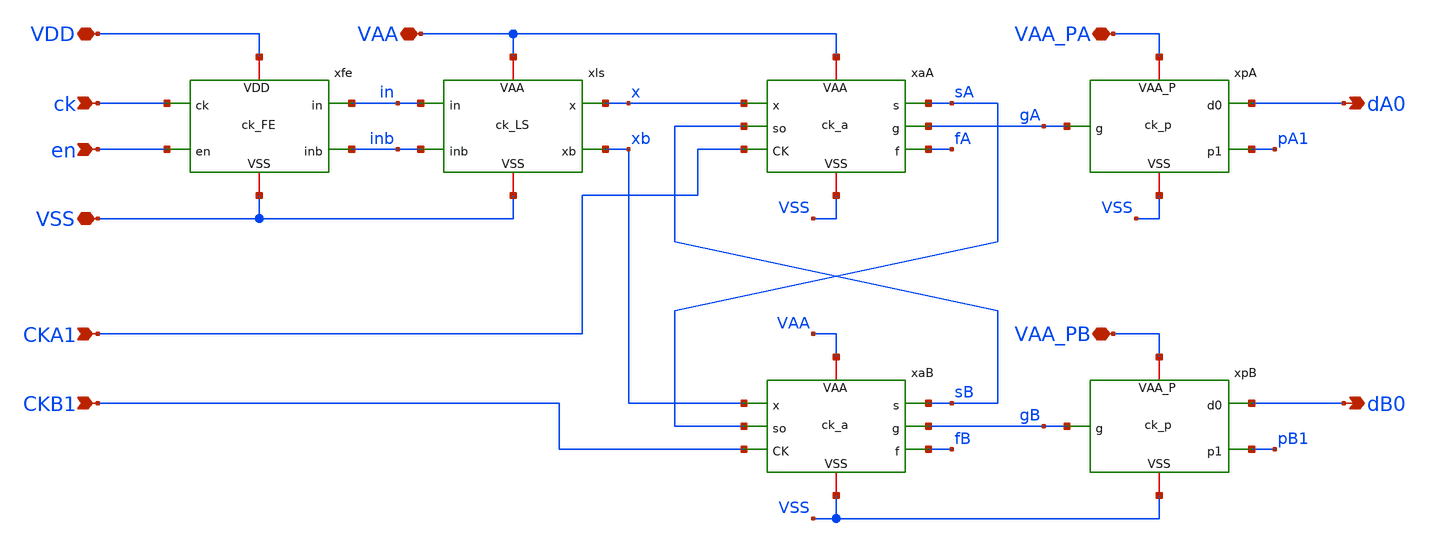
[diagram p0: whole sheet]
** sch_path: xschem/clkblock.sch
**.subckt clkblock VSS dA0 dB0 ck en VDD VAA VAA_PA VAA_PB CKA1 CKB1
*.iopin VSS
*.opin dA0
*.opin dB0
*.ipin ck
*.ipin en
*.iopin VDD
*.iopin VAA
*.iopin VAA_PA
*.iopin VAA_PB
*.ipin CKA1
*.ipin CKB1
xfe ck en inb in VSS VDD ck_FE
xls in inb x xb VSS VAA ck_LS
xaA gA sB x CKA1 fA sA VSS VAA ck_a
xaB gB sA xb CKB1 fB sB VSS VAA ck_a
xpA gA pA1 dA0 VSS VAA_PA ck_p
xpB gB pB1 dB0 VSS VAA_PB ck_p
**.ends

* expanding   symbol:  ck_FE.sym # of pins=6
** sym_path: xschem/ck_FE.sym
** sch_path: xschem/ck_FE.sch
.subckt ck_FE ck en inb in VSS VDD
*.iopin VDD
*.iopin VSS
*.ipin ck
*.ipin en
*.opin in
*.opin inb
XPN1 inb ck VDD VDD pfet_03v3 L=1.12u W=2.0u nf=1 ad='int((nf+1)/2) * W/nf * 0.18u' as='int((nf+2)/2) * W/nf * 0.18u'
+ pd='2*int((nf+1)/2) * (W/nf + 0.18u)' ps='2*int((nf+2)/2) * (W/nf + 0.18u)' nrd='0.18u / W' nrs='0.18u / W'
+ sa=0 sb=0 sd=0 m=1 par=1
XPN2 inb en VDD VDD pfet_03v3 L=1.12u W=2.0u nf=1 ad='int((nf+1)/2) * W/nf * 0.18u' as='int((nf+2)/2) * W/nf * 0.18u'
+ pd='2*int((nf+1)/2) * (W/nf + 0.18u)' ps='2*int((nf+2)/2) * (W/nf + 0.18u)' nrd='0.18u / W' nrs='0.18u / W'
+ sa=0 sb=0 sd=0 m=1 par=1
XNN1 inb ck nn VSS nfet_03v3 L=1.12u W=2.0u nf=1 ad='int((nf+1)/2) * W/nf * 0.18u' as='int((nf+2)/2) * W/nf * 0.18u'
+ pd='2*int((nf+1)/2) * (W/nf + 0.18u)' ps='2*int((nf+2)/2) * (W/nf + 0.18u)' nrd='0.18u / W' nrs='0.18u / W'
+ sa=0 sb=0 sd=0 m=1 par=1
XNN2 nn en VSS VSS nfet_03v3 L=1.12u W=2.0u nf=1 ad='int((nf+1)/2) * W/nf * 0.18u' as='int((nf+2)/2) * W/nf * 0.18u'
+ pd='2*int((nf+1)/2) * (W/nf + 0.18u)' ps='2*int((nf+2)/2) * (W/nf + 0.18u)' nrd='0.18u / W' nrs='0.18u / W'
+ sa=0 sb=0 sd=0 m=1 par=1
XPI1 in inb VDD VDD pfet_03v3 L=1.12u W=2.00u nf=1 ad='int((nf+1)/2) * W/nf * 0.18u' as='int((nf+2)/2) * W/nf * 0.18u'
+ pd='2*int((nf+1)/2) * (W/nf + 0.18u)' ps='2*int((nf+2)/2) * (W/nf + 0.18u)' nrd='0.18u / W' nrs='0.18u / W'
+ sa=0 sb=0 sd=0 m=1 par=1
XNI1 in inb VSS VSS nfet_03v3 L=1.12u W=1.0u nf=1 ad='int((nf+1)/2) * W/nf * 0.18u' as='int((nf+2)/2) * W/nf * 0.18u'
+ pd='2*int((nf+1)/2) * (W/nf + 0.18u)' ps='2*int((nf+2)/2) * (W/nf + 0.18u)' nrd='0.18u / W' nrs='0.18u / W'
+ sa=0 sb=0 sd=0 m=1 par=1
.ends


* expanding   symbol:  ck_LS.sym # of pins=6
** sym_path: xschem/ck_LS.sym
** sch_path: xschem/ck_LS.sch
.subckt ck_LS in inb x xb VSS VAA
*.ipin in
*.ipin inb
*.opin x
*.opin xb
*.iopin VSS
*.iopin VAA
XLP1 x xb VAA VAA pfet_06v0 L=2.2u W=1.0u nf=1 ad='int((nf+1)/2) * W/nf * 0.18u' as='int((nf+2)/2) * W/nf * 0.18u'
+ pd='2*int((nf+1)/2) * (W/nf + 0.18u)' ps='2*int((nf+2)/2) * (W/nf + 0.18u)' nrd='0.18u / W' nrs='0.18u / W'
+ sa=0 sb=0 sd=0 m=1
XLP2 xb x VAA VAA pfet_06v0 L=2.2u W=1.0u nf=1 ad='int((nf+1)/2) * W/nf * 0.18u' as='int((nf+2)/2) * W/nf * 0.18u'
+ pd='2*int((nf+1)/2) * (W/nf + 0.18u)' ps='2*int((nf+2)/2) * (W/nf + 0.18u)' nrd='0.18u / W' nrs='0.18u / W'
+ sa=0 sb=0 sd=0 m=1
XLN1 x in VSS VSS nfet_06v0 L=0.7u W=1.0u nf=1 ad='int((nf+1)/2) * W/nf * 0.18u' as='int((nf+2)/2) * W/nf * 0.18u'
+ pd='2*int((nf+1)/2) * (W/nf + 0.18u)' ps='2*int((nf+2)/2) * (W/nf + 0.18u)' nrd='0.18u / W' nrs='0.18u / W'
+ sa=0 sb=0 sd=0 m=1 par=1
XLN2 xb inb VSS VSS nfet_06v0 L=0.7u W=1.0u nf=1 ad='int((nf+1)/2) * W/nf * 0.18u' as='int((nf+2)/2) * W/nf * 0.18u'
+ pd='2*int((nf+1)/2) * (W/nf + 0.18u)' ps='2*int((nf+2)/2) * (W/nf + 0.18u)' nrd='0.18u / W' nrs='0.18u / W'
+ sa=0 sb=0 sd=0 m=1 par=1
.ends


* expanding   symbol:  ck_a.sym # of pins=8
** sym_path: xschem/ck_a.sym
** sch_path: xschem/ck_a.sch
.subckt ck_a g so x CK f s VSS VAA
*.ipin so
*.iopin VAA
*.iopin VSS
*.ipin x
*.opin g
*.ipin CK
*.opin f
*.opin s
XPA m x VAA VAA pfet_06v0 L=0.55u W=5.0u nf=2 ad='int((nf+1)/2) * W/nf * 0.18u' as='int((nf+2)/2) * W/nf * 0.18u'
+ pd='2*int((nf+1)/2) * (W/nf + 0.18u)' ps='2*int((nf+2)/2) * (W/nf + 0.18u)' nrd='0.18u / W' nrs='0.18u / W'
+ sa=0 sb=0 sd=0 m=1
XPB g so m VAA pfet_06v0 L=0.55u W=5.0u nf=2 ad='int((nf+1)/2) * W/nf * 0.18u' as='int((nf+2)/2) * W/nf * 0.18u'
+ pd='2*int((nf+1)/2) * (W/nf + 0.18u)' ps='2*int((nf+2)/2) * (W/nf + 0.18u)' nrd='0.18u / W' nrs='0.18u / W'
+ sa=0 sb=0 sd=0 m=1
XNA g x VSS VSS nfet_06v0 L=0.70u W=1.0u nf=1 ad='int((nf+1)/2) * W/nf * 0.18u' as='int((nf+2)/2) * W/nf * 0.18u'
+ pd='2*int((nf+1)/2) * (W/nf + 0.18u)' ps='2*int((nf+2)/2) * (W/nf + 0.18u)' nrd='0.18u / W' nrs='0.18u / W'
+ sa=0 sb=0 sd=0 m=1 par=1
XNB g so VSS VSS nfet_06v0 L=0.70u W=1.0u nf=1 ad='int((nf+1)/2) * W/nf * 0.18u' as='int((nf+2)/2) * W/nf * 0.18u'
+ pd='2*int((nf+1)/2) * (W/nf + 0.18u)' ps='2*int((nf+2)/2) * (W/nf + 0.18u)' nrd='0.18u / W' nrs='0.18u / W'
+ sa=0 sb=0 sd=0 m=1 par=1
XPSN f CK VAA VAA pfet_06v0 L=0.55u W=0.4u nf=1 ad='int((nf+1)/2) * W/nf * 0.18u' as='int((nf+2)/2) * W/nf * 0.18u'
+ pd='2*int((nf+1)/2) * (W/nf + 0.18u)' ps='2*int((nf+2)/2) * (W/nf + 0.18u)' nrd='0.18u / W' nrs='0.18u / W'
+ sa=0 sb=0 sd=0 m=1
XNSN f CK VSS VSS nfet_06v0 L=0.70u W=8.0u nf=4 ad='int((nf+1)/2) * W/nf * 0.18u' as='int((nf+2)/2) * W/nf * 0.18u'
+ pd='2*int((nf+1)/2) * (W/nf + 0.18u)' ps='2*int((nf+2)/2) * (W/nf + 0.18u)' nrd='0.18u / W' nrs='0.18u / W'
+ sa=0 sb=0 sd=0 m=1 par=1
XPF s f VAA VAA pfet_06v0 L=0.55u W=2.5u nf=1 ad='int((nf+1)/2) * W/nf * 0.18u' as='int((nf+2)/2) * W/nf * 0.18u'
+ pd='2*int((nf+1)/2) * (W/nf + 0.18u)' ps='2*int((nf+2)/2) * (W/nf + 0.18u)' nrd='0.18u / W' nrs='0.18u / W'
+ sa=0 sb=0 sd=0 m=1
XNF s f VSS VSS nfet_06v0 L=0.70u W=1.0u nf=1 ad='int((nf+1)/2) * W/nf * 0.18u' as='int((nf+2)/2) * W/nf * 0.18u'
+ pd='2*int((nf+1)/2) * (W/nf + 0.18u)' ps='2*int((nf+2)/2) * (W/nf + 0.18u)' nrd='0.18u / W' nrs='0.18u / W'
+ sa=0 sb=0 sd=0 m=1 par=1
.ends


* expanding   symbol:  ck_p.sym # of pins=5
** sym_path: xschem/ck_p.sym
** sch_path: xschem/ck_p.sch
.subckt ck_p g p1 d0 VSS VAA_P
*.ipin g
*.iopin VAA_P
*.opin d0
*.opin p1
*.iopin VSS
XPP1 p1 g VAA_P VAA_P pfet_06v0 L=0.55u W=2.5u nf=1 ad='int((nf+1)/2) * W/nf * 0.18u' as='int((nf+2)/2) * W/nf * 0.18u'
+ pd='2*int((nf+1)/2) * (W/nf + 0.18u)' ps='2*int((nf+2)/2) * (W/nf + 0.18u)' nrd='0.18u / W' nrs='0.18u / W'
+ sa=0 sb=0 sd=0 m=1
XPP2 d0 p1 VAA_P VAA_P pfet_06v0 L=0.55u W=7.5u nf=3 ad='int((nf+1)/2) * W/nf * 0.18u' as='int((nf+2)/2) * W/nf * 0.18u'
+ pd='2*int((nf+1)/2) * (W/nf + 0.18u)' ps='2*int((nf+2)/2) * (W/nf + 0.18u)' nrd='0.18u / W' nrs='0.18u / W'
+ sa=0 sb=0 sd=0 m=1
XNP1 p1 g VSS VSS nfet_06v0 L=0.70u W=1.0u nf=1 ad='int((nf+1)/2) * W/nf * 0.18u' as='int((nf+2)/2) * W/nf * 0.18u'
+ pd='2*int((nf+1)/2) * (W/nf + 0.18u)' ps='2*int((nf+2)/2) * (W/nf + 0.18u)' nrd='0.18u / W' nrs='0.18u / W'
+ sa=0 sb=0 sd=0 m=1 par=1
XNP2 d0 p1 VSS VSS nfet_06v0 L=0.70u W=3.0u nf=3 ad='int((nf+1)/2) * W/nf * 0.18u' as='int((nf+2)/2) * W/nf * 0.18u'
+ pd='2*int((nf+1)/2) * (W/nf + 0.18u)' ps='2*int((nf+2)/2) * (W/nf + 0.18u)' nrd='0.18u / W' nrs='0.18u / W'
+ sa=0 sb=0 sd=0 m=1 par=1
.ends

.end
